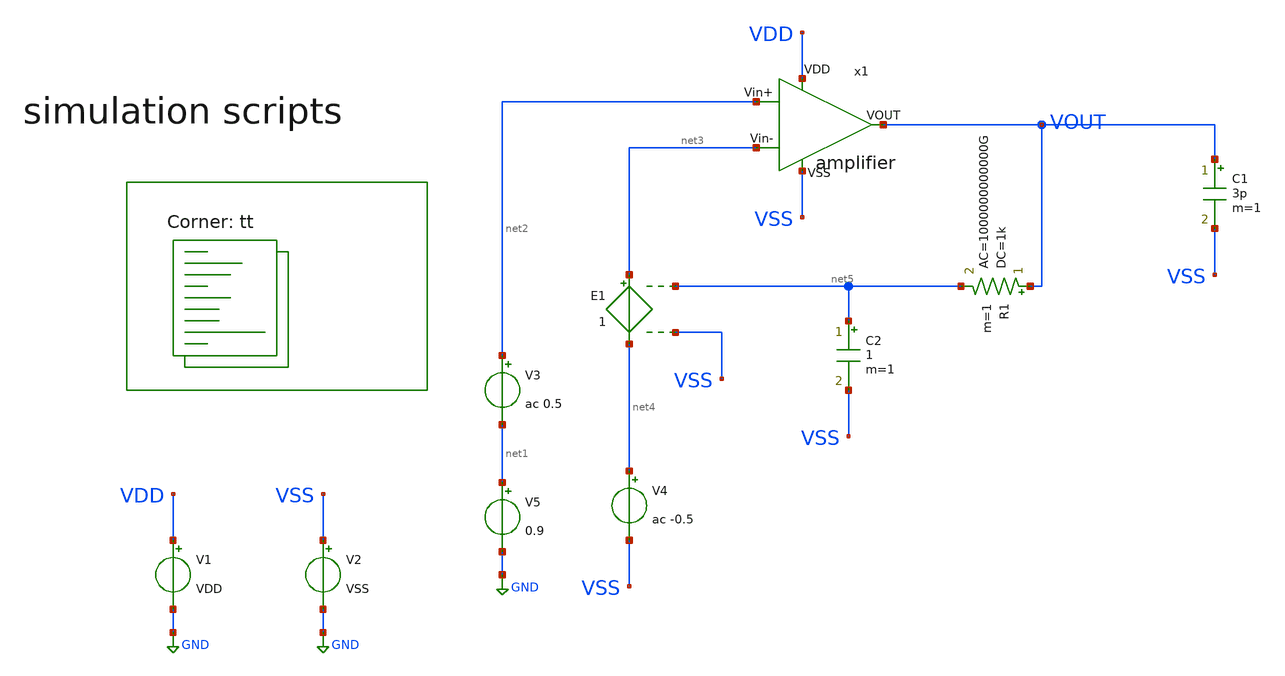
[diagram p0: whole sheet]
** sch_path: Learning/single_ended_amplifiers/Design_and_Analysis_of_Two-Stage_CMOS_Operational_Amplifier_for_Fluorescence_Signal_Processing_sky130_1_8V/amplifier/tb.sch
**.subckt tb
x1 VDD VSS net2 net3 VOUT amplifier
V1 VDD GND VDD
V2 VSS GND VSS
V5 net1 GND 0.9
V3 net2 net1 ac 0.5
V4 net4 VSS ac -0.5
E1 net3 net4 net5 VSS 1
C1 VOUT VSS 3p m=1
R1 VOUT net5 1k ac=1000000000000G m=1
C2 net5 VSS 1 m=1
**** begin user architecture code
.lib $::SKYWATER_MODELS/sky130.lib.spice tt
**** end user architecture code
**.ends

* expanding   symbol:  Sky130A/Learning/Design_of_two_stage_CMOS_MILLER_OTA_1_8/amplifier.sym # of
*+ pins=5
** sym_path: my_ip/LIB/Sky130A/Learning/Design_of_two_stage_CMOS_MILLER_OTA_1_8/amplifier.sym
** sch_path: my_ip/LIB/Sky130A/Learning/Design_of_two_stage_CMOS_MILLER_OTA_1_8/amplifier.sch
.subckt amplifier VDD VSS Vin+ Vin- VOUT
*.iopin VDD
*.iopin VSS
*.iopin Vin+
*.iopin Vin-
*.iopin VOUT
XR6 VSS net3 VSS sky130_fd_pr__res_high_po_0p35 L=16 mult=1 m=1
XM1 net1 net2 net3 VSS sky130_fd_pr__nfet_01v8 L=4 W='1 * 8 ' nf=8 ad='int((8 + 1)/2) * 1 / 8 * 0.29'
+ as='int((8 + 2)/2) * 1 / 8 * 0.29' pd='2*int((8 + 1)/2) * (1 / 8 + 0.29)' ps='2*int((8 + 2)/2) * (1 / 8 + 0.29)'
+ nrd='0.29 / 1 ' nrs='0.29 / 1 ' sa=0 sb=0 sd=0 mult=2 m=2
XM2 net2 net2 VSS VSS sky130_fd_pr__nfet_01v8 L=4 W='1 * 2 ' nf=2 ad='int((2 + 1)/2) * 1 / 2 * 0.29'
+ as='int((2 + 2)/2) * 1 / 2 * 0.29' pd='2*int((2 + 1)/2) * (1 / 2 + 0.29)' ps='2*int((2 + 2)/2) * (1 / 2 + 0.29)'
+ nrd='0.29 / 1 ' nrs='0.29 / 1 ' sa=0 sb=0 sd=0 mult=2 m=2
XM4 VB2 VB2 net2 VSS sky130_fd_pr__nfet_01v8_lvt L=2 W='1 * 2 ' nf=2 ad='int((2 + 1)/2) * 1 / 2 * 0.29'
+ as='int((2 + 2)/2) * 1 / 2 * 0.29' pd='2*int((2 + 1)/2) * (1 / 2 + 0.29)' ps='2*int((2 + 2)/2) * (1 / 2 + 0.29)'
+ nrd='0.29 / 1 ' nrs='0.29 / 1 ' sa=0 sb=0 sd=0 mult=2 m=2
XM3 VB1 VB2 net1 VSS sky130_fd_pr__nfet_01v8_lvt L=2 W='1 * 2 ' nf=2 ad='int((2 + 1)/2) * 1 / 2 * 0.29'
+ as='int((2 + 2)/2) * 1 / 2 * 0.29' pd='2*int((2 + 1)/2) * (1 / 2 + 0.29)' ps='2*int((2 + 2)/2) * (1 / 2 + 0.29)'
+ nrd='0.29 / 1 ' nrs='0.29 / 1 ' sa=0 sb=0 sd=0 mult=2 m=2
XM5 VB1 VB1 VDD VDD sky130_fd_pr__pfet_01v8 L=2 W='1 * 2 ' nf=2 ad= as='int((2 + 2)/2) * 1 * 0.29' pd='2*int((2 + 1)/2) * (1 + 0.29)'
+ ps='2*int((2 + 2)/2) * (1 + 0.29)' nrd='0.29 / 1 / 2 ' nrs='0.29 / 1 / 2 ' sa=0 sb=0 sd=0 mult=2 m=2
XM6 VB2 VB1 VDD VDD sky130_fd_pr__pfet_01v8 L=2 W='1 * 2 ' nf=2 ad= as='int((2 + 2)/2) * 1 * 0.29' pd='2*int((2 + 1)/2) * (1 + 0.29)'
+ ps='2*int((2 + 2)/2) * (1 + 0.29)' nrd='0.29 / 1 / 2 ' nrs='0.29 / 1 / 2 ' sa=0 sb=0 sd=0 mult=2 m=2
XM7 net4 VB1 VDD VDD sky130_fd_pr__pfet_01v8 L=2 W='1 * 2 ' nf=2 ad= as='int((2 + 2)/2) * 1 * 0.29' pd='2*int((2 + 1)/2) * (1 + 0.29)'
+ ps='2*int((2 + 2)/2) * (1 + 0.29)' nrd='0.29 / 1 / 2 ' nrs='0.29 / 1 / 2 ' sa=0 sb=0 sd=0 mult=8 m=8
XM10 net5 net5 VSS VSS sky130_fd_pr__nfet_01v8 L=2 W='1 * 2 ' nf=2 ad='int((2 + 1)/2) * 1 / 2 * 0.29'
+ as='int((2 + 2)/2) * 1 / 2 * 0.29' pd='2*int((2 + 1)/2) * (1 / 2 + 0.29)' ps='2*int((2 + 2)/2) * (1 / 2 + 0.29)'
+ nrd='0.29 / 1 ' nrs='0.29 / 1 ' sa=0 sb=0 sd=0 mult=2 m=2
XM11 net6 net5 VSS VSS sky130_fd_pr__nfet_01v8 L=2 W='1 * 2 ' nf=2 ad='int((2 + 1)/2) * 1 / 2 * 0.29'
+ as='int((2 + 2)/2) * 1 / 2 * 0.29' pd='2*int((2 + 1)/2) * (1 / 2 + 0.29)' ps='2*int((2 + 2)/2) * (1 / 2 + 0.29)'
+ nrd='0.29 / 1 ' nrs='0.29 / 1 ' sa=0 sb=0 sd=0 mult=2 m=2
XM12 VOUT VB1 VDD VDD sky130_fd_pr__pfet_01v8 L=2 W='1 * 2 ' nf=2 ad= as='int((2 + 2)/2) * 1 * 0.29'
+ pd='2*int((2 + 1)/2) * (1 + 0.29)' ps='2*int((2 + 2)/2) * (1 + 0.29)' nrd='0.29 / 1 / 2 ' nrs='0.29 / 1 / 2 '
+ sa=0 sb=0 sd=0 mult=16 m=16
XM14 net7 VB2 net6 VSS sky130_fd_pr__nfet_01v8 L=2.2 W='2 * 1 ' nf=1 ad='int((1 + 1)/2) * 2 / 1 * 0.29'
+ as='int((1 + 2)/2) * 2 / 1 * 0.29' pd='2*int((1 + 1)/2) * (2 / 1 + 0.29)' ps='2*int((1 + 2)/2) * (2 / 1 + 0.29)'
+ nrd='0.29 / 2 ' nrs='0.29 / 2 ' sa=0 sb=0 sd=0 mult=2 m=2
XC1 VOUT net7 sky130_fd_pr__cap_mim_m3_1 W=6.5 L=6.5 MF=4 m=4
XM8 net5 Vin- net4 net4 sky130_fd_pr__pfet_01v8_lvt L=0.7 W='2 * 2 ' nf=2 ad='int((2 + 1)/2) * 2 / 2 * 0.29'
+ as='int((2 + 2)/2) * 2 / 2 * 0.29' pd='2*int((2 + 1)/2) * (2 / 2 + 0.29)' ps='2*int((2 + 2)/2) * (2 / 2 + 0.29)'
+ nrd='0.29 / 2 ' nrs='0.29 / 2 ' sa=0 sb=0 sd=0 mult=4 m=4
XM9 net6 Vin+ net4 net4 sky130_fd_pr__pfet_01v8_lvt L=0.7 W='2 * 2 ' nf=2 ad='int((2 + 1)/2) * 2 / 2 * 0.29'
+ as='int((2 + 2)/2) * 2 / 2 * 0.29' pd='2*int((2 + 1)/2) * (2 / 2 + 0.29)' ps='2*int((2 + 2)/2) * (2 / 2 + 0.29)'
+ nrd='0.29 / 2 ' nrs='0.29 / 2 ' sa=0 sb=0 sd=0 mult=4 m=4
XM33 VOUT net6 VSS VSS sky130_fd_pr__nfet_01v8_lvt L=0.5 W='2 * 2 ' nf=2 ad='int((2 + 1)/2) * 2 / 2 * 0.29'
+ as='int((2 + 2)/2) * 2 / 2 * 0.29' pd='2*int((2 + 1)/2) * (2 / 2 + 0.29)' ps='2*int((2 + 2)/2) * (2 / 2 + 0.29)'
+ nrd='0.29 / 2 ' nrs='0.29 / 2 ' sa=0 sb=0 sd=0 mult=2 m=2
.ends

.GLOBAL GND
**** begin user architecture code




.Temp 27
.param VDD = 1.8
.param VSS = 0


.control
save all
op
print @m.x1.xm9.msky130_fd_pr__pfet_01v8_lvt[vth]
print @m.x1.xm9.msky130_fd_pr__pfet_01v8_lvt[gm]
print 1/@m.x1.xm9.msky130_fd_pr__pfet_01v8_lvt[gds]
print @m.x1.xm9.msky130_fd_pr__pfet_01v8_lvt[vdsat]
print @m.x1.xm9.msky130_fd_pr__pfet_01v8_lvt[cdg]


print @m.x1.xm11.msky130_fd_pr__nfet_01v8[vth]
print @m.x1.xm11.msky130_fd_pr__nfet_01v8[gm]
print 1/@m.x1.xm11.msky130_fd_pr__nfet_01v8[gds]
print @m.x1.xm11.msky130_fd_pr__nfet_01v8[vdsat]
print @m.x1.xm11.msky130_fd_pr__nfet_01v8[cdg]

print @m.x1.xm13.msky130_fd_pr__nfet_01v8[vth]
print @m.x1.xm13.msky130_fd_pr__nfet_01v8[gm]
print 1/@m.x1.xm13.msky130_fd_pr__nfet_01v8[gds]
print @m.x1.xm13.msky130_fd_pr__nfet_01v8[vdsat]
print @m.x1.xm13.msky130_fd_pr__nfet_01v8[cdg]


print @m.x1.xm12.msky130_fd_pr__pfet_01v8[vth]
print @m.x1.xm12.msky130_fd_pr__pfet_01v8[gm]
print 1/@m.x1.xm12.msky130_fd_pr__pfet_01v8[gds]
print @m.x1.xm12.msky130_fd_pr__pfet_01v8[vdsat]
print @m.x1.xm12.msky130_fd_pr__pfet_01v8[cdg]

print 1.8*I(V2)

ac dec 1000 1 10G
plot db(v(VOUT)) (180+(180*ph(v(VOUT))/pi))



.endc



**** end user architecture code
.end
